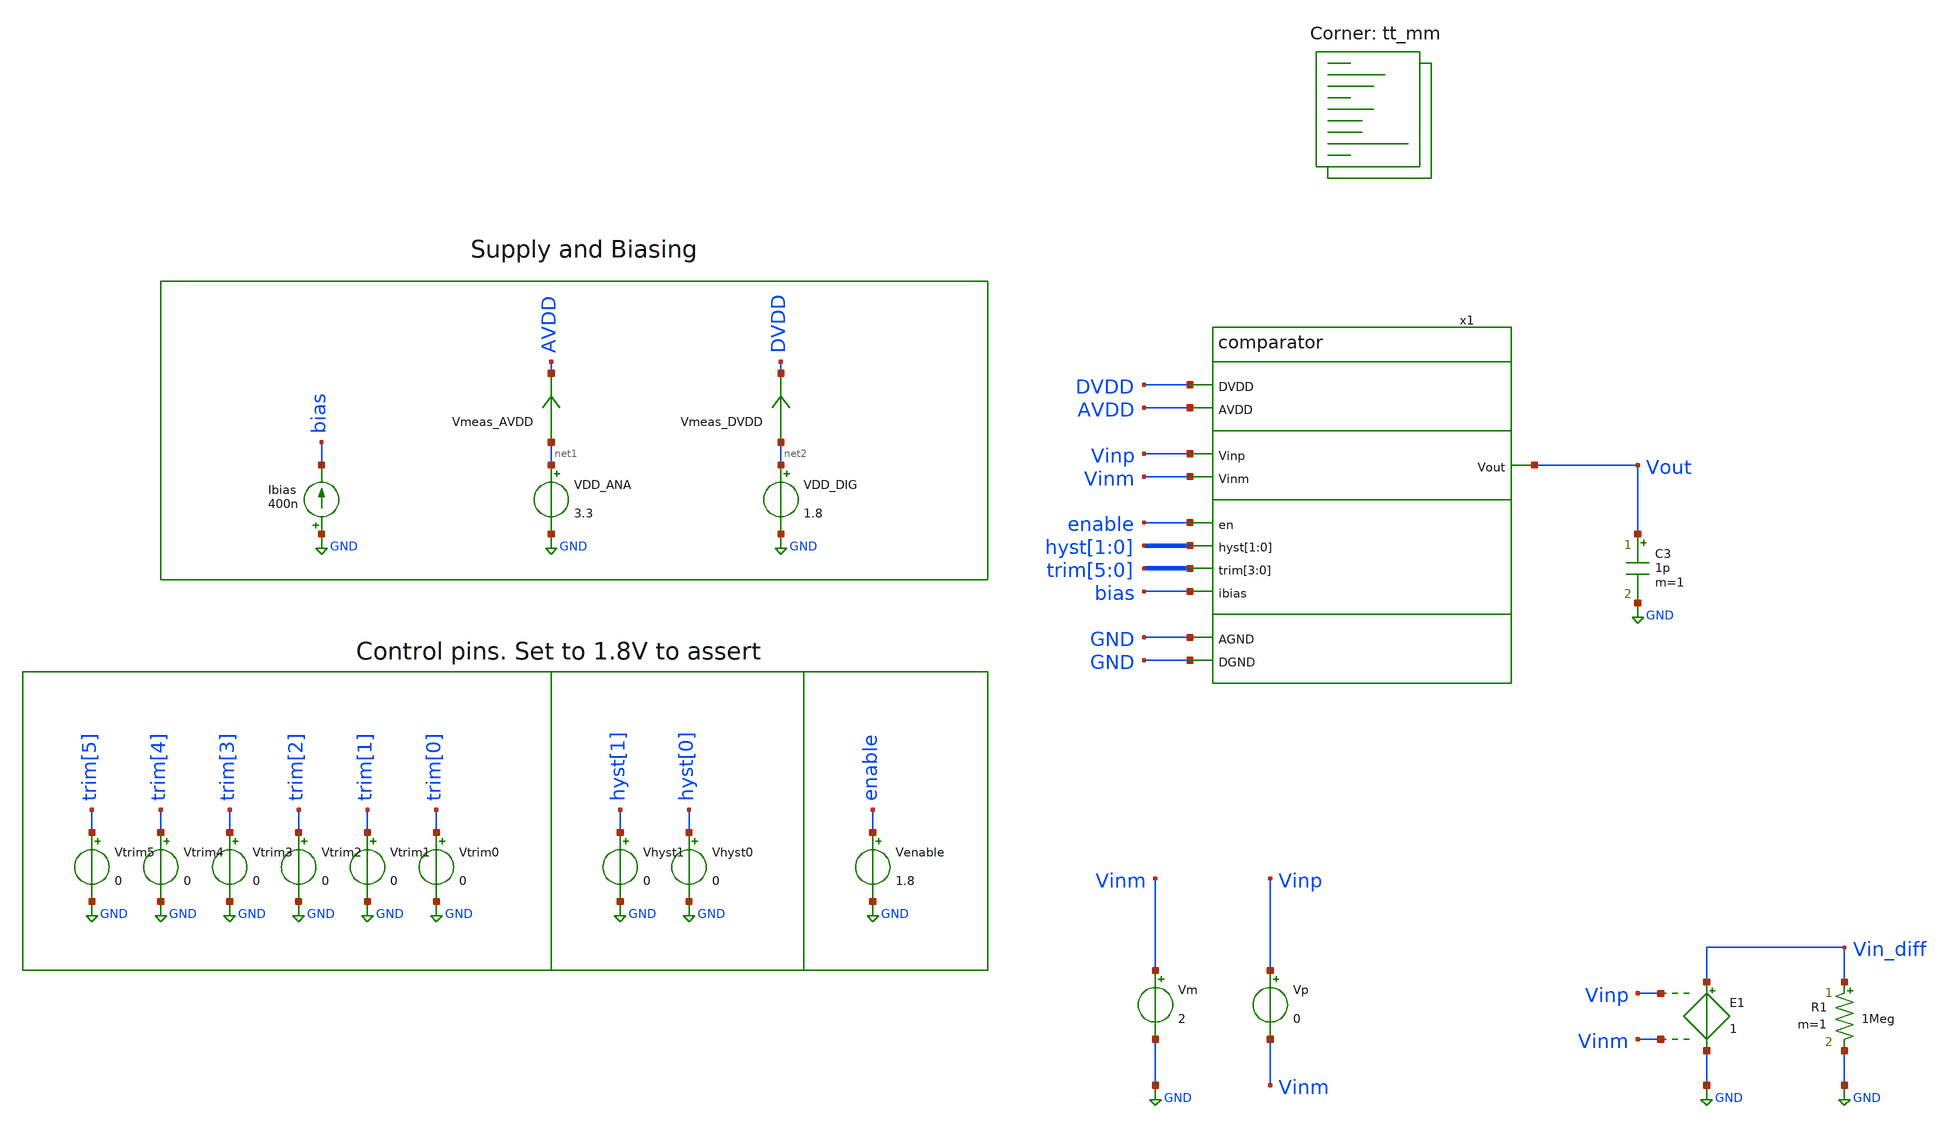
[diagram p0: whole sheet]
** sch_path: xschem/tb_comparator_offset.sch
**.subckt tb_comparator_offset
Vp Vinp Vinm 0
VDD_ANA net1 GND 3.3
VDD_DIG net2 GND 1.8
Ibias GND bias 400n
C3 Vout GND 1p m=1
Vm Vinm GND 2
Vmeas_AVDD net1 AVDD 0
.save i(vmeas_avdd)
Vmeas_DVDD net2 DVDD 0
.save i(vmeas_dvdd)
E1 Vin_diff GND Vinp Vinm 1
R1 Vin_diff GND 1Meg m=1
Vtrim3 trim[3] GND 0
Vtrim2 trim[2] GND 0
Vtrim1 trim[1] GND 0
Vtrim0 trim[0] GND 0
Vhyst1 hyst[1] GND 0
Vhyst0 hyst[0] GND 0
Venable enable GND 1.8
Vtrim5 trim[5] GND 0
Vtrim4 trim[4] GND 0
x1 DVDD AVDD GND GND Vinp Vout Vinm enable hyst[1] hyst[0] trim[5] trim[4] trim[3] trim[2] bias
+ comparator
**** begin user architecture code
.lib $::SKYWATER_MODELS/sky130.lib.spice tt_mm


.save v(vout)
.dc Vp -10m 10m 0.10m
.param TEMPGAUSS = agauss(40, 30, 1)
.option temp='TEMPGAUSS'
*.option temp=27

.control
   let num_meas = 50
   let input_offset = unitvec(num_meas)
   let i = 0
   dowhile i<num_meas
      option seed=8
      run
      meas dc in_cross when v(vout)=0.9 rise=1
      let input_offset[i] = in_cross
      let i = i+1
      reset
   end
plot dc1.v(vout) dc2.v(vout) dc3.v(vout) dc4.v(vout) dc5.v(vout) dc6.v(vout) dc7.v(vout) dc8.v(vout)
+ dc9.v(vout) dc10.v(vout) dc11.v(vout) dc12.v(vout) dc13.v(vout) dc14.v(vout) dc15.v(vout) dc16.v(vout)
+ dc17.v(vout) dc18.v(vout) dc19.v(vout) dc20.v(vout) dc21.v(vout) dc21.v(vout) dc22.v(vout) dc23.v(vout)
+ dc24.v(vout) dc25.v(vout)
*plot tran1.v(vinp)
set filetype = ascii
write results.raw input_offset
print vecmax(input_offset)
print vecmin(input_offset)
.endc


**** end user architecture code
**.ends
.GLOBAL GND
.end
